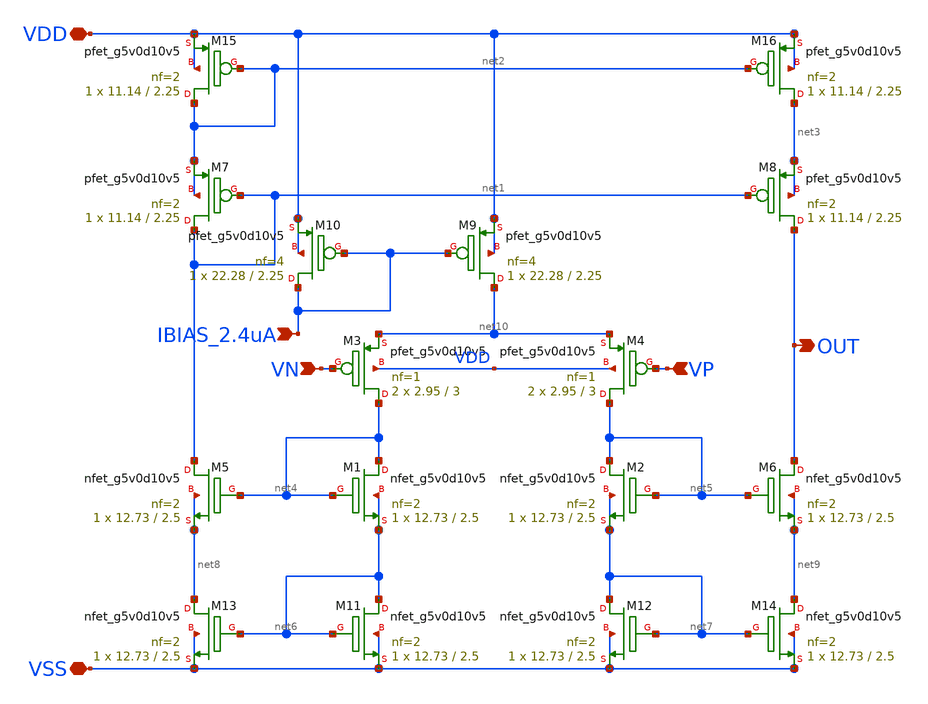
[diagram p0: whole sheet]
** sch_path: xschem/error_amplifier.sch
**.subckt error_amplifier VSS IBIAS_2.4uA OUT VN VP VDD
*.iopin VSS
*.ipin IBIAS_2.4uA
*.opin OUT
*.ipin VN
*.ipin VP
*.iopin VDD
XM1 net4 net4 net6 net6 sky130_fd_pr__nfet_g5v0d10v5 L=2.5 W=12.73 nf=2 ad='int((nf+1)/2) * W/nf * 0.29'
+ as='int((nf+2)/2) * W/nf * 0.29' pd='2*int((nf+1)/2) * (W/nf + 0.29)' ps='2*int((nf+2)/2) * (W/nf + 0.29)'
+ nrd='0.29 / W' nrs='0.29 / W' sa=0 sb=0 sd=0 mult=1 m=1
XM2 net5 net5 net7 net7 sky130_fd_pr__nfet_g5v0d10v5 L=2.5 W=12.73 nf=2 ad='int((nf+1)/2) * W/nf * 0.29'
+ as='int((nf+2)/2) * W/nf * 0.29' pd='2*int((nf+1)/2) * (W/nf + 0.29)' ps='2*int((nf+2)/2) * (W/nf + 0.29)'
+ nrd='0.29 / W' nrs='0.29 / W' sa=0 sb=0 sd=0 mult=1 m=1
XM3 net4 VN net10 VDD sky130_fd_pr__pfet_g5v0d10v5 L=3 W=2.95 nf=1 ad='int((nf+1)/2) * W/nf * 0.29' as='int((nf+2)/2) * W/nf * 0.29'
+ pd='2*int((nf+1)/2) * (W/nf + 0.29)' ps='2*int((nf+2)/2) * (W/nf + 0.29)' nrd='0.29 / W' nrs='0.29 / W'
+ sa=0 sb=0 sd=0 mult=2 m=2
XM4 net5 VP net10 VDD sky130_fd_pr__pfet_g5v0d10v5 L=3 W=2.95 nf=1 ad='int((nf+1)/2) * W/nf * 0.29' as='int((nf+2)/2) * W/nf * 0.29'
+ pd='2*int((nf+1)/2) * (W/nf + 0.29)' ps='2*int((nf+2)/2) * (W/nf + 0.29)' nrd='0.29 / W' nrs='0.29 / W'
+ sa=0 sb=0 sd=0 mult=2 m=2
XM5 net1 net4 net8 net8 sky130_fd_pr__nfet_g5v0d10v5 L=2.5 W=12.73 nf=2 ad='int((nf+1)/2) * W/nf * 0.29'
+ as='int((nf+2)/2) * W/nf * 0.29' pd='2*int((nf+1)/2) * (W/nf + 0.29)' ps='2*int((nf+2)/2) * (W/nf + 0.29)'
+ nrd='0.29 / W' nrs='0.29 / W' sa=0 sb=0 sd=0 mult=1 m=1
XM6 OUT net5 net9 net9 sky130_fd_pr__nfet_g5v0d10v5 L=2.5 W=12.73 nf=2 ad='int((nf+1)/2) * W/nf * 0.29'
+ as='int((nf+2)/2) * W/nf * 0.29' pd='2*int((nf+1)/2) * (W/nf + 0.29)' ps='2*int((nf+2)/2) * (W/nf + 0.29)'
+ nrd='0.29 / W' nrs='0.29 / W' sa=0 sb=0 sd=0 mult=1 m=1
XM9 net10 IBIAS_2.4uA VDD VDD sky130_fd_pr__pfet_g5v0d10v5 L=2.25 W=22.28 nf=4 ad='int((nf+1)/2) * W/nf * 0.29'
+ as='int((nf+2)/2) * W/nf * 0.29' pd='2*int((nf+1)/2) * (W/nf + 0.29)' ps='2*int((nf+2)/2) * (W/nf + 0.29)'
+ nrd='0.29 / W' nrs='0.29 / W' sa=0 sb=0 sd=0 mult=1 m=1
XM10 IBIAS_2.4uA IBIAS_2.4uA VDD VDD sky130_fd_pr__pfet_g5v0d10v5 L=2.25 W=22.28 nf=4 ad='int((nf+1)/2) * W/nf * 0.29'
+ as='int((nf+2)/2) * W/nf * 0.29' pd='2*int((nf+1)/2) * (W/nf + 0.29)' ps='2*int((nf+2)/2) * (W/nf + 0.29)'
+ nrd='0.29 / W' nrs='0.29 / W' sa=0 sb=0 sd=0 mult=1 m=1
XM7 net1 net1 net2 net2 sky130_fd_pr__pfet_g5v0d10v5 L=2.25 W=11.14 nf=2 ad='int((nf+1)/2) * W/nf * 0.29'
+ as='int((nf+2)/2) * W/nf * 0.29' pd='2*int((nf+1)/2) * (W/nf + 0.29)' ps='2*int((nf+2)/2) * (W/nf + 0.29)'
+ nrd='0.29 / W' nrs='0.29 / W' sa=0 sb=0 sd=0 mult=1 m=1
XM8 OUT net1 net3 net3 sky130_fd_pr__pfet_g5v0d10v5 L=2.25 W=11.14 nf=2 ad='int((nf+1)/2) * W/nf * 0.29'
+ as='int((nf+2)/2) * W/nf * 0.29' pd='2*int((nf+1)/2) * (W/nf + 0.29)' ps='2*int((nf+2)/2) * (W/nf + 0.29)'
+ nrd='0.29 / W' nrs='0.29 / W' sa=0 sb=0 sd=0 mult=1 m=1
XM11 net6 net6 VSS VSS sky130_fd_pr__nfet_g5v0d10v5 L=2.5 W=12.73 nf=2 ad='int((nf+1)/2) * W/nf * 0.29'
+ as='int((nf+2)/2) * W/nf * 0.29' pd='2*int((nf+1)/2) * (W/nf + 0.29)' ps='2*int((nf+2)/2) * (W/nf + 0.29)'
+ nrd='0.29 / W' nrs='0.29 / W' sa=0 sb=0 sd=0 mult=1 m=1
XM12 net7 net7 VSS VSS sky130_fd_pr__nfet_g5v0d10v5 L=2.5 W=12.73 nf=2 ad='int((nf+1)/2) * W/nf * 0.29'
+ as='int((nf+2)/2) * W/nf * 0.29' pd='2*int((nf+1)/2) * (W/nf + 0.29)' ps='2*int((nf+2)/2) * (W/nf + 0.29)'
+ nrd='0.29 / W' nrs='0.29 / W' sa=0 sb=0 sd=0 mult=1 m=1
XM13 net8 net6 VSS VSS sky130_fd_pr__nfet_g5v0d10v5 L=2.5 W=12.73 nf=2 ad='int((nf+1)/2) * W/nf * 0.29'
+ as='int((nf+2)/2) * W/nf * 0.29' pd='2*int((nf+1)/2) * (W/nf + 0.29)' ps='2*int((nf+2)/2) * (W/nf + 0.29)'
+ nrd='0.29 / W' nrs='0.29 / W' sa=0 sb=0 sd=0 mult=1 m=1
XM14 net9 net7 VSS VSS sky130_fd_pr__nfet_g5v0d10v5 L=2.5 W=12.73 nf=2 ad='int((nf+1)/2) * W/nf * 0.29'
+ as='int((nf+2)/2) * W/nf * 0.29' pd='2*int((nf+1)/2) * (W/nf + 0.29)' ps='2*int((nf+2)/2) * (W/nf + 0.29)'
+ nrd='0.29 / W' nrs='0.29 / W' sa=0 sb=0 sd=0 mult=1 m=1
XM15 net2 net2 VDD VDD sky130_fd_pr__pfet_g5v0d10v5 L=2.25 W=11.14 nf=2 ad='int((nf+1)/2) * W/nf * 0.29'
+ as='int((nf+2)/2) * W/nf * 0.29' pd='2*int((nf+1)/2) * (W/nf + 0.29)' ps='2*int((nf+2)/2) * (W/nf + 0.29)'
+ nrd='0.29 / W' nrs='0.29 / W' sa=0 sb=0 sd=0 mult=1 m=1
XM16 net3 net2 VDD VDD sky130_fd_pr__pfet_g5v0d10v5 L=2.25 W=11.14 nf=2 ad='int((nf+1)/2) * W/nf * 0.29'
+ as='int((nf+2)/2) * W/nf * 0.29' pd='2*int((nf+1)/2) * (W/nf + 0.29)' ps='2*int((nf+2)/2) * (W/nf + 0.29)'
+ nrd='0.29 / W' nrs='0.29 / W' sa=0 sb=0 sd=0 mult=1 m=1
**.ends
.end
